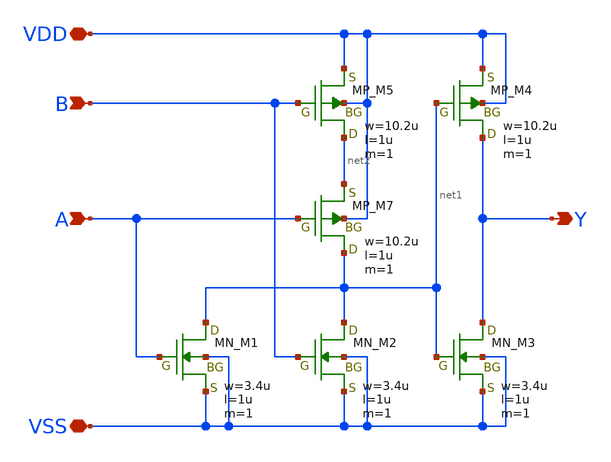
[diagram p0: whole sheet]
** sch_path: member_project/imager/YuMaehashi/design/pulsegen_or2.sch
**.subckt pulsegen_or2 A B Y VDD VSS
*.ipin A
*.ipin B
*.opin Y
*.iopin VDD
*.iopin VSS
XM7 net1 A net2 VDD PMOS w=10.2u l=1u as=0 ad=0 ps=0 pd=0 nrd=0 nrs=0 m=1
XM1 net1 A VSS VSS NMOS w=3.4u l=1u as=0 ad=0 ps=0 pd=0 nrd=0 nrs=0 m=1
XM2 net1 B VSS VSS NMOS w=3.4u l=1u as=0 ad=0 ps=0 pd=0 nrd=0 nrs=0 m=1
XM3 Y net1 VSS VSS NMOS w=3.4u l=1u as=0 ad=0 ps=0 pd=0 nrd=0 nrs=0 m=1
XM4 Y net1 VDD VDD PMOS w=10.2u l=1u as=0 ad=0 ps=0 pd=0 nrd=0 nrs=0 m=1
XM5 net2 B VDD VDD PMOS w=10.2u l=1u as=0 ad=0 ps=0 pd=0 nrd=0 nrs=0 m=1
**.ends
.end
